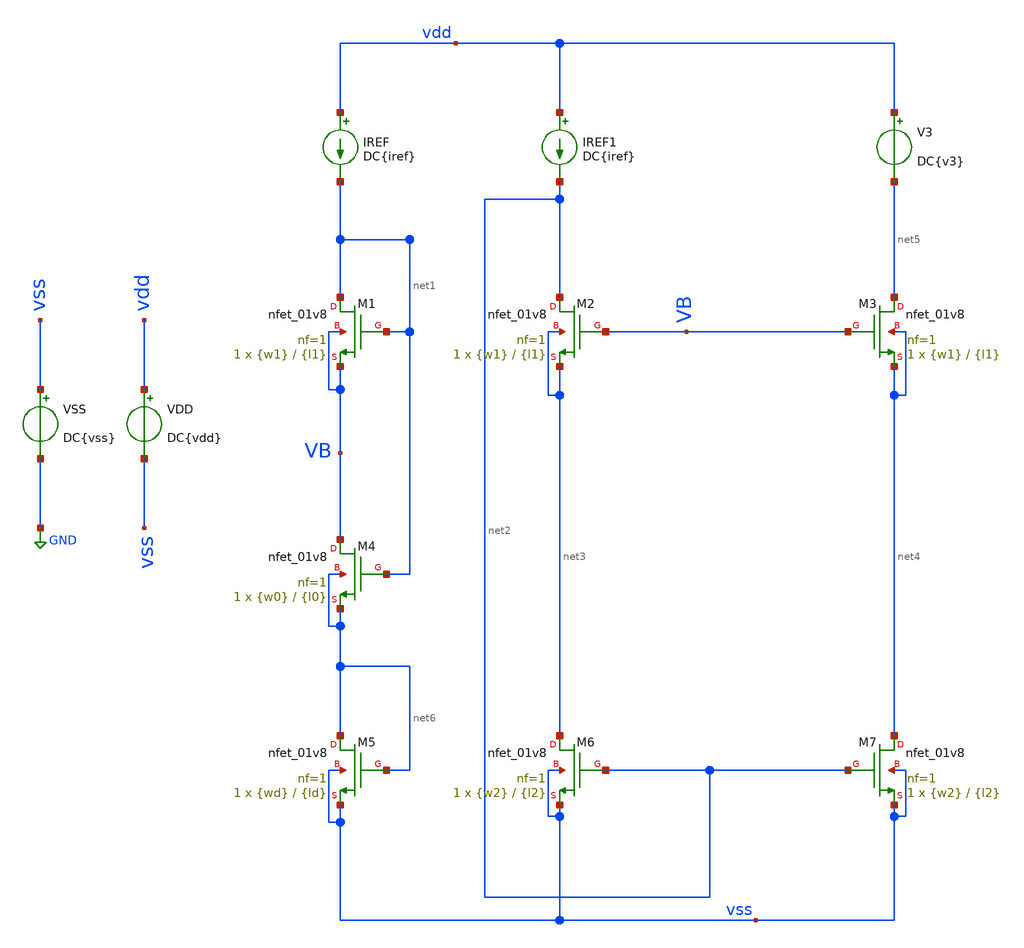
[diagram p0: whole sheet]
** sch_path: Tp2/Mis Simulaciones/tp2_3b.sch
**.subckt tp2_3b
XM1 net1 net1 VB VB sky130_fd_pr__nfet_01v8 L={l1} W={w1} nf=1 ad='int((nf+1)/2) * W/nf * 0.29' as='int((nf+2)/2) * W/nf * 0.29'
+ pd='2*int((nf+1)/2) * (W/nf + 0.29)' ps='2*int((nf+2)/2) * (W/nf + 0.29)' nrd='0.29 / W' nrs='0.29 / W'
+ sa=0 sb=0 sd=0 mult=1 m=1
XM2 net2 VB net3 net3 sky130_fd_pr__nfet_01v8 L={l1} W={w1} nf=1 ad='int((nf+1)/2) * W/nf * 0.29' as='int((nf+2)/2) * W/nf * 0.29'
+ pd='2*int((nf+1)/2) * (W/nf + 0.29)' ps='2*int((nf+2)/2) * (W/nf + 0.29)' nrd='0.29 / W' nrs='0.29 / W'
+ sa=0 sb=0 sd=0 mult=1 m=1
IREF vdd net1 DC{iref}
VSS vss GND DC{vss}
VDD vdd vss DC{vdd}
XM3 net5 VB net4 net4 sky130_fd_pr__nfet_01v8 L={l1} W={w1} nf=1 ad='int((nf+1)/2) * W/nf * 0.29' as='int((nf+2)/2) * W/nf * 0.29'
+ pd='2*int((nf+1)/2) * (W/nf + 0.29)' ps='2*int((nf+2)/2) * (W/nf + 0.29)' nrd='0.29 / W' nrs='0.29 / W'
+ sa=0 sb=0 sd=0 mult=1 m=1
XM5 net6 net6 vss vss sky130_fd_pr__nfet_01v8 L={ld} W={wd} nf=1 ad='int((nf+1)/2) * W/nf * 0.29' as='int((nf+2)/2) * W/nf * 0.29'
+ pd='2*int((nf+1)/2) * (W/nf + 0.29)' ps='2*int((nf+2)/2) * (W/nf + 0.29)' nrd='0.29 / W' nrs='0.29 / W'
+ sa=0 sb=0 sd=0 mult=1 m=1
XM6 net3 net2 vss vss sky130_fd_pr__nfet_01v8 L={l2} W={w2} nf=1 ad='int((nf+1)/2) * W/nf * 0.29' as='int((nf+2)/2) * W/nf * 0.29'
+ pd='2*int((nf+1)/2) * (W/nf + 0.29)' ps='2*int((nf+2)/2) * (W/nf + 0.29)' nrd='0.29 / W' nrs='0.29 / W'
+ sa=0 sb=0 sd=0 mult=1 m=1
XM7 net4 net2 vss vss sky130_fd_pr__nfet_01v8 L={l2} W={w2} nf=1 ad='int((nf+1)/2) * W/nf * 0.29' as='int((nf+2)/2) * W/nf * 0.29'
+ pd='2*int((nf+1)/2) * (W/nf + 0.29)' ps='2*int((nf+2)/2) * (W/nf + 0.29)' nrd='0.29 / W' nrs='0.29 / W'
+ sa=0 sb=0 sd=0 mult=1 m=1
V3 vdd net5 DC{v3}
IREF1 vdd net2 DC{iref}
XM4 VB net1 net6 net6 sky130_fd_pr__nfet_01v8 L={l0} W={w0} nf=1 ad='int((nf+1)/2) * W/nf * 0.29' as='int((nf+2)/2) * W/nf * 0.29'
+ pd='2*int((nf+1)/2) * (W/nf + 0.29)' ps='2*int((nf+2)/2) * (W/nf + 0.29)' nrd='0.29 / W' nrs='0.29 / W'
+ sa=0 sb=0 sd=0 mult=1 m=1
**** begin user architecture code



* Parameters
.param vdd = 1.8
.param vss = 0.0
.param iref = 200u
.param v3 = 1.2
.param l2 = 0.9
.param l1 = 0.15
.param l0 = 0.15
.param wd = 30
.param ld = 3
.param w0 = 1
.param w1 = 10
.param w2 = 10
.options TEMPS = 27.0

* Models
.lib ~/skywater/skywater-pdk/libraries/sky130_fd_pr_ngspice/latest/models/corners/sky130.lib TT

* Data to save
.save all  @M.XM1.msky130_fd_pr__nfet_01v8[id]  @M.XM1.msky130_fd_pr__nfet_01v8[vth]  @M.XM1.msky130_fd_pr__nfet_01v8[vdsat]  @M.XM1.msky130_fd_pr__nfet_01v8[gm]  @M.XM1.msky130_fd_pr__nfet_01v8[vds]  @M.XM1.msky130_fd_pr__nfet_01v8[vgs]  @M.XM1.msky130_fd_pr__nfet_01v8[w]  @M.XM2.msky130_fd_pr__nfet_01v8[id]  @M.XM2.msky130_fd_pr__nfet_01v8[vth]  @M.XM2.msky130_fd_pr__nfet_01v8[vdsat]  @M.XM2.msky130_fd_pr__nfet_01v8[gm]  @M.XM2.msky130_fd_pr__nfet_01v8[vds]  @M.XM2.msky130_fd_pr__nfet_01v8[vgs]  @M.XM2.msky130_fd_pr__nfet_01v8[w]  @M.XM3.msky130_fd_pr__nfet_01v8[id]  @M.XM3.msky130_fd_pr__nfet_01v8[vth]  @M.XM3.msky130_fd_pr__nfet_01v8[vdsat]  @M.XM3.msky130_fd_pr__nfet_01v8[gm]  @M.XM3.msky130_fd_pr__nfet_01v8[vds]  @M.XM3.msky130_fd_pr__nfet_01v8[vgs]  @M.XM3.msky130_fd_pr__nfet_01v8[w]  @M.XM4.msky130_fd_pr__nfet_01v8[id]  @M.XM4.msky130_fd_pr__nfet_01v8[vth]  @M.XM4.msky130_fd_pr__nfet_01v8[vdsat]  @M.XM4.msky130_fd_pr__nfet_01v8[gm]  @M.XM4.msky130_fd_pr__nfet_01v8[vds]  @M.XM4.msky130_fd_pr__nfet_01v8[vgs]  @M.XM4.msky130_fd_pr__nfet_01v8[w]  @M.XM5.msky130_fd_pr__nfet_01v8[id]  @M.XM5.msky130_fd_pr__nfet_01v8[vth]  @M.XM5.msky130_fd_pr__nfet_01v8[vdsat]  @M.XM5.msky130_fd_pr__nfet_01v8[gm]  @M.XM5.msky130_fd_pr__nfet_01v8[vds]  @M.XM5.msky130_fd_pr__nfet_01v8[vgs]  @M.XM5.msky130_fd_pr__nfet_01v8[w]  @M.XM6.msky130_fd_pr__nfet_01v8[id]  @M.XM6.msky130_fd_pr__nfet_01v8[vth]  @M.XM6.msky130_fd_pr__nfet_01v8[vdsat]  @M.XM6.msky130_fd_pr__nfet_01v8[gm]  @M.XM6.msky130_fd_pr__nfet_01v8[vds]  @M.XM6.msky130_fd_pr__nfet_01v8[vgs]  @M.XM6.msky130_fd_pr__nfet_01v8[w]  @M.XM7.msky130_fd_pr__nfet_01v8[id]  @M.XM7.msky130_fd_pr__nfet_01v8[vth]  @M.XM7.msky130_fd_pr__nfet_01v8[vdsat]  @M.XM7.msky130_fd_pr__nfet_01v8[gm]  @M.XM7.msky130_fd_pr__nfet_01v8[vds]  @M.XM7.msky130_fd_pr__nfet_01v8[vgs]  @M.XM7.msky130_fd_pr__nfet_01v8[w]

* Simulation
.control
  *let wi = 1.5
  *let wf = 4.5
  *let wstep = 0.15

  *dowhile wi <= wf
    *print @M.XM1.msky130_fd_pr__nfet_01v8[w]
    *alter @M.XM1.msky130_fd_pr__nfet_01v8[w] = wi
    *alter @M.XM2.msky130_fd_pr__nfet_01v8[w] = wi
    *let wi = wi + wstep
    *op
    *print @M.XM1.msky130_fd_pr__nfet_01v8[w]
    *print @M.XM1.msky130_fd_pr__nfet_01v8[id]
    *print @M.XM1.msky130_fd_pr__nfet_01v8[vds]
    *print @M.XM1.msky130_fd_pr__nfet_01v8[vgs]
    *print @M.XM2.msky130_fd_pr__nfet_01v8[w]
    *print @M.XM2.msky130_fd_pr__nfet_01v8[id]
    *print @M.XM2.msky130_fd_pr__nfet_01v8[vds]
    *print @M.XM2.msky130_fd_pr__nfet_01v8[vgs]
    *print @M.XM3.msky130_fd_pr__nfet_01v8[w]
    *print @M.XM3.msky130_fd_pr__nfet_01v8[id]
    *print @M.XM3.msky130_fd_pr__nfet_01v8[vds]
    *print @M.XM3.msky130_fd_pr__nfet_01v8[vgs]
    *print @M.XM4.msky130_fd_pr__nfet_01v8[w]
    *print @M.XM4.msky130_fd_pr__nfet_01v8[id]
    *print @M.XM4.msky130_fd_pr__nfet_01v8[vds]
    *print @M.XM4.msky130_fd_pr__nfet_01v8[vgs]
    *print @M.XM5.msky130_fd_pr__nfet_01v8[w]
    *print @M.XM5.msky130_fd_pr__nfet_01v8[id]
    *print @M.XM5.msky130_fd_pr__nfet_01v8[vds]
    *print @M.XM5.msky130_fd_pr__nfet_01v8[vgs]
    *print @M.XM6.msky130_fd_pr__nfet_01v8[w]
    *print @M.XM6.msky130_fd_pr__nfet_01v8[id]
    *print @M.XM6.msky130_fd_pr__nfet_01v8[vds]
    *print @M.XM6.msky130_fd_pr__nfet_01v8[vgs]
    *print @M.XM7.msky130_fd_pr__nfet_01v8[w]
    *print @M.XM7.msky130_fd_pr__nfet_01v8[id]
    *print @M.XM7.msky130_fd_pr__nfet_01v8[vds]
    *print @M.XM7.msky130_fd_pr__nfet_01v8[vgs]
    *save all
  *end
  *write tp2_3b.raw

  unset filetype
  op
  save all
  write tp2_3b.raw

.endc

.end


**** end user architecture code
**.ends
.GLOBAL GND
.end
